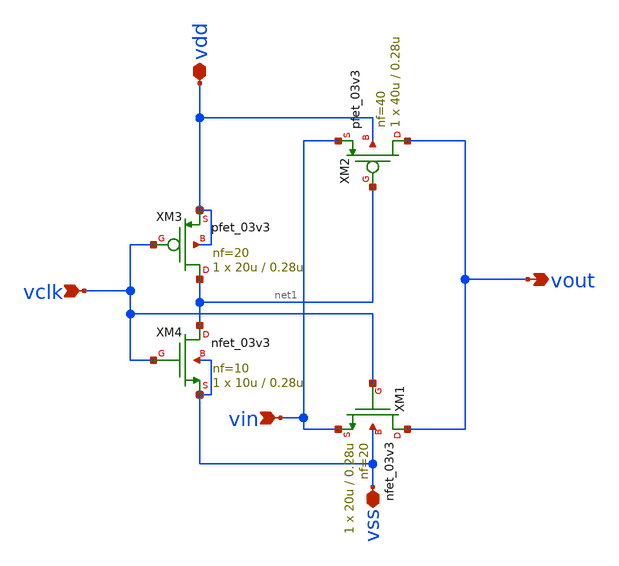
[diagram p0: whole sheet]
** sch_path: analog/blocks/transmission_gate/transmission_gate.sch
**.subckt transmission_gate vclk vin vdd vss vout
*.ipin vclk
*.ipin vin
*.iopin vdd
*.iopin vss
*.opin vout
XM1 vout vclk vin vss nfet_03v3 L=0.28u W=20u nf=20 ad='int((nf+1)/2) * W/nf * 0.18u' as='int((nf+2)/2) * W/nf * 0.18u'
+ pd='2*int((nf+1)/2) * (W/nf + 0.18u)' ps='2*int((nf+2)/2) * (W/nf + 0.18u)' nrd='0.18u / W' nrs='0.18u / W'
+ sa=0 sb=0 sd=0 m=1
XM2 vout net1 vin vdd pfet_03v3 L=0.28u W=40u nf=40 ad='int((nf+1)/2) * W/nf * 0.18u' as='int((nf+2)/2) * W/nf * 0.18u'
+ pd='2*int((nf+1)/2) * (W/nf + 0.18u)' ps='2*int((nf+2)/2) * (W/nf + 0.18u)' nrd='0.18u / W' nrs='0.18u / W'
+ sa=0 sb=0 sd=0 m=1
XM3 net1 vclk vdd vdd pfet_03v3 L=0.28u W=20u nf=20 ad='int((nf+1)/2) * W/nf * 0.18u' as='int((nf+2)/2) * W/nf * 0.18u'
+ pd='2*int((nf+1)/2) * (W/nf + 0.18u)' ps='2*int((nf+2)/2) * (W/nf + 0.18u)' nrd='0.18u / W' nrs='0.18u / W'
+ sa=0 sb=0 sd=0 m=1
XM4 net1 vclk vss vss nfet_03v3 L=0.28u W=10u nf=10 ad='int((nf+1)/2) * W/nf * 0.18u' as='int((nf+2)/2) * W/nf * 0.18u'
+ pd='2*int((nf+1)/2) * (W/nf + 0.18u)' ps='2*int((nf+2)/2) * (W/nf + 0.18u)' nrd='0.18u / W' nrs='0.18u / W'
+ sa=0 sb=0 sd=0 m=1
**.ends
.end
